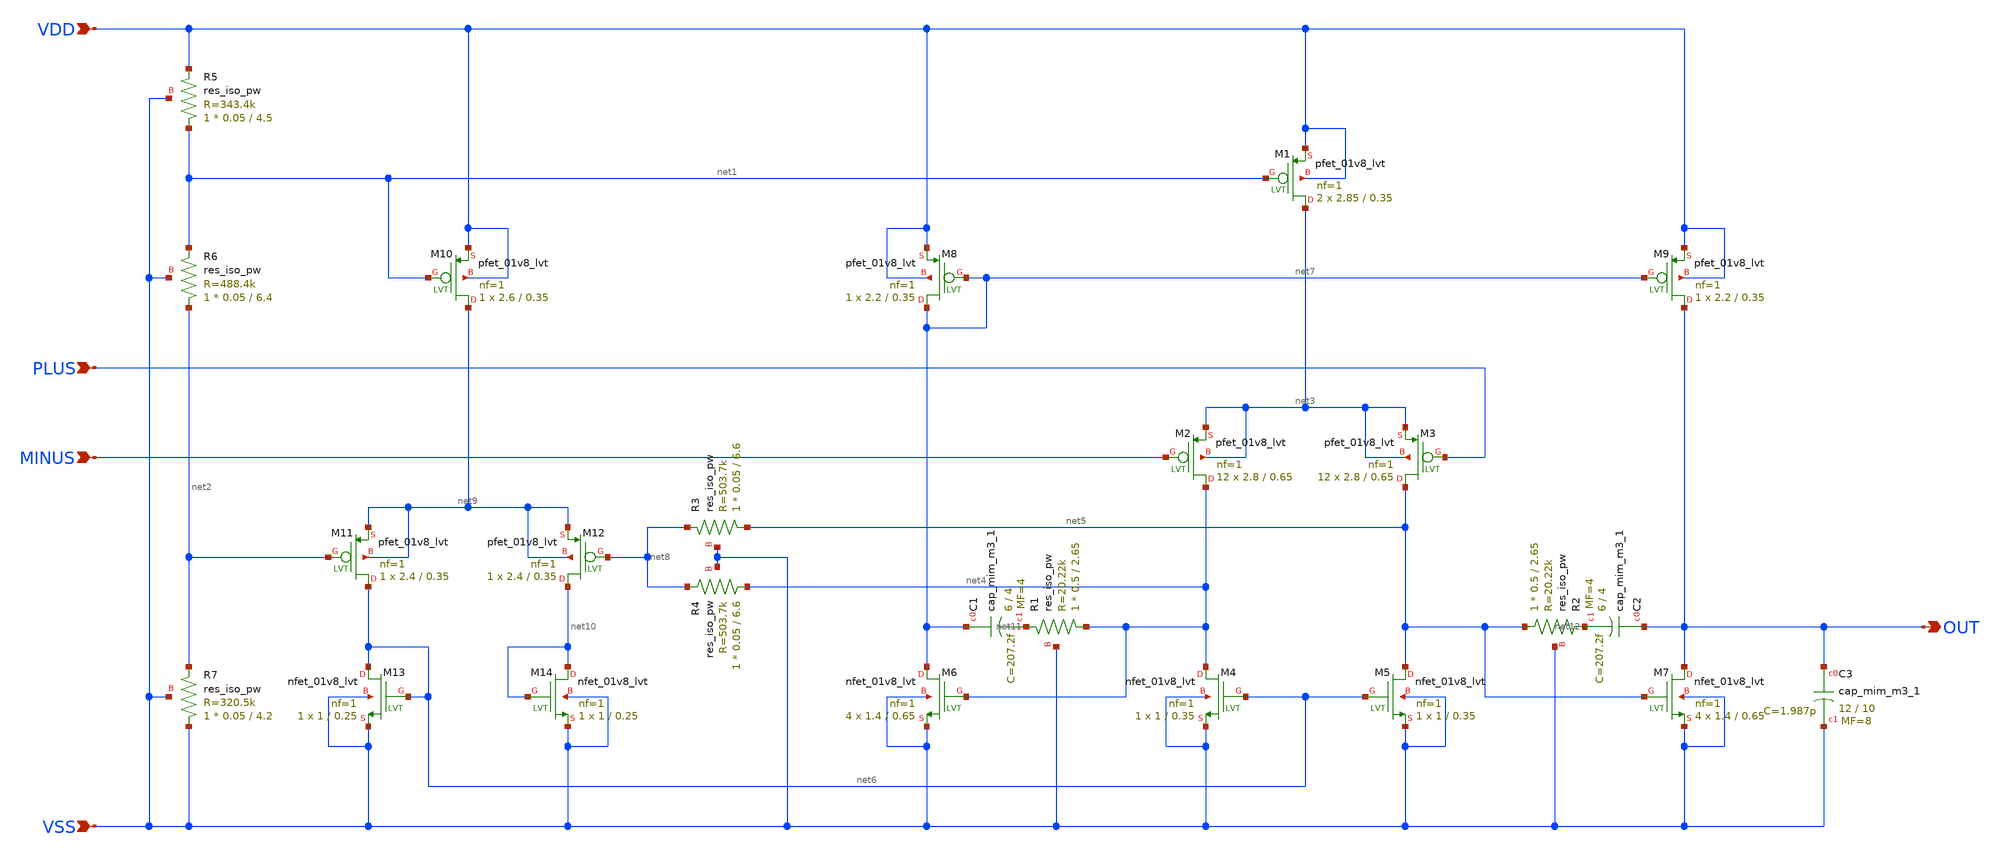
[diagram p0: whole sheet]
** sch_path: schematic/opamp.sch
**.subckt opamp VDD VSS PLUS MINUS OUT
*.ipin VDD
*.ipin VSS
*.ipin PLUS
*.ipin MINUS
*.opin OUT
XM1 net3 net1 VDD VDD sky130_fd_pr__pfet_01v8_lvt L=0.35 W=2.85 nf=1 ad='int((1 + 1)/2) * 2.85 / 1 * 0.29'
+ as='int((1 + 2)/2) * 2.85 / 1 * 0.29' pd='2*int((1 + 1)/2) * (2.85 / 1 + 0.29)' ps='2*int((1 + 2)/2) * (2.85 / 1 + 0.29)'
+ nrd='0.29 / 2.85 ' nrs='0.29 / 2.85 ' sa=0 sb=0 sd=0 mult=2 m=2
XM2 net4 MINUS net3 net3 sky130_fd_pr__pfet_01v8_lvt L=0.65 W=2.8 nf=1 ad='int((1 + 1)/2) * 2.8 / 1 * 0.29'
+ as='int((1 + 2)/2) * 2.8 / 1 * 0.29' pd='2*int((1 + 1)/2) * (2.8 / 1 + 0.29)' ps='2*int((1 + 2)/2) * (2.8 / 1 + 0.29)'
+ nrd='0.29 / 2.8 ' nrs='0.29 / 2.8 ' sa=0 sb=0 sd=0 mult=12 m=12
XM3 net5 PLUS net3 net3 sky130_fd_pr__pfet_01v8_lvt L=0.65 W=2.8 nf=1 ad='int((1 + 1)/2) * 2.8 / 1 * 0.29'
+ as='int((1 + 2)/2) * 2.8 / 1 * 0.29' pd='2*int((1 + 1)/2) * (2.8 / 1 + 0.29)' ps='2*int((1 + 2)/2) * (2.8 / 1 + 0.29)'
+ nrd='0.29 / 2.8 ' nrs='0.29 / 2.8 ' sa=0 sb=0 sd=0 mult=12 m=12
XM4 net4 net6 VSS VSS sky130_fd_pr__nfet_01v8_lvt L=0.35 W=1 nf=1 ad='int((1 + 1)/2) * 1 / 1 * 0.29'
+ as='int((1 + 2)/2) * 1 / 1 * 0.29' pd='2*int((1 + 1)/2) * (1 / 1 + 0.29)' ps='2*int((1 + 2)/2) * (1 / 1 + 0.29)'
+ nrd='0.29 / 1 ' nrs='0.29 / 1 ' sa=0 sb=0 sd=0 mult=1 m=1
XM5 net5 net6 VSS VSS sky130_fd_pr__nfet_01v8_lvt L=0.35 W=1 nf=1 ad='int((1 + 1)/2) * 1 / 1 * 0.29'
+ as='int((1 + 2)/2) * 1 / 1 * 0.29' pd='2*int((1 + 1)/2) * (1 / 1 + 0.29)' ps='2*int((1 + 2)/2) * (1 / 1 + 0.29)'
+ nrd='0.29 / 1 ' nrs='0.29 / 1 ' sa=0 sb=0 sd=0 mult=1 m=1
XM6 net7 net4 VSS VSS sky130_fd_pr__nfet_01v8_lvt L=0.65 W=1.4 nf=1 ad='int((1 + 1)/2) * 1.4 / 1 * 0.29'
+ as='int((1 + 2)/2) * 1.4 / 1 * 0.29' pd='2*int((1 + 1)/2) * (1.4 / 1 + 0.29)' ps='2*int((1 + 2)/2) * (1.4 / 1 + 0.29)'
+ nrd='0.29 / 1.4 ' nrs='0.29 / 1.4 ' sa=0 sb=0 sd=0 mult=4 m=4
XM7 OUT net5 VSS VSS sky130_fd_pr__nfet_01v8_lvt L=0.65 W=1.4 nf=1 ad='int((1 + 1)/2) * 1.4 / 1 * 0.29'
+ as='int((1 + 2)/2) * 1.4 / 1 * 0.29' pd='2*int((1 + 1)/2) * (1.4 / 1 + 0.29)' ps='2*int((1 + 2)/2) * (1.4 / 1 + 0.29)'
+ nrd='0.29 / 1.4 ' nrs='0.29 / 1.4 ' sa=0 sb=0 sd=0 mult=4 m=4
XM8 net7 net7 VDD VDD sky130_fd_pr__pfet_01v8_lvt L=0.35 W=2.2 nf=1 ad='int((1 + 1)/2) * 2.2 / 1 * 0.29'
+ as='int((1 + 2)/2) * 2.2 / 1 * 0.29' pd='2*int((1 + 1)/2) * (2.2 / 1 + 0.29)' ps='2*int((1 + 2)/2) * (2.2 / 1 + 0.29)'
+ nrd='0.29 / 2.2 ' nrs='0.29 / 2.2 ' sa=0 sb=0 sd=0 mult=1 m=1
XM9 OUT net7 VDD VDD sky130_fd_pr__pfet_01v8_lvt L=0.35 W=2.2 nf=1 ad='int((1 + 1)/2) * 2.2 / 1 * 0.29'
+ as='int((1 + 2)/2) * 2.2 / 1 * 0.29' pd='2*int((1 + 1)/2) * (2.2 / 1 + 0.29)' ps='2*int((1 + 2)/2) * (2.2 / 1 + 0.29)'
+ nrd='0.29 / 2.2 ' nrs='0.29 / 2.2 ' sa=0 sb=0 sd=0 mult=1 m=1
XM10 net9 net1 VDD VDD sky130_fd_pr__pfet_01v8_lvt L=0.35 W=2.6 nf=1 ad='int((1 + 1)/2) * 2.6 / 1 * 0.29'
+ as='int((1 + 2)/2) * 2.6 / 1 * 0.29' pd='2*int((1 + 1)/2) * (2.6 / 1 + 0.29)' ps='2*int((1 + 2)/2) * (2.6 / 1 + 0.29)'
+ nrd='0.29 / 2.6 ' nrs='0.29 / 2.6 ' sa=0 sb=0 sd=0 mult=1 m=1
XM11 net6 net2 net9 net9 sky130_fd_pr__pfet_01v8_lvt L=0.35 W=2.4 nf=1 ad='int((1 + 1)/2) * 2.4 / 1 * 0.29'
+ as='int((1 + 2)/2) * 2.4 / 1 * 0.29' pd='2*int((1 + 1)/2) * (2.4 / 1 + 0.29)' ps='2*int((1 + 2)/2) * (2.4 / 1 + 0.29)'
+ nrd='0.29 / 2.4 ' nrs='0.29 / 2.4 ' sa=0 sb=0 sd=0 mult=1 m=1
XM12 net10 net8 net9 net9 sky130_fd_pr__pfet_01v8_lvt L=0.35 W=2.4 nf=1 ad='int((1 + 1)/2) * 2.4 / 1 * 0.29'
+ as='int((1 + 2)/2) * 2.4 / 1 * 0.29' pd='2*int((1 + 1)/2) * (2.4 / 1 + 0.29)' ps='2*int((1 + 2)/2) * (2.4 / 1 + 0.29)'
+ nrd='0.29 / 2.4 ' nrs='0.29 / 2.4 ' sa=0 sb=0 sd=0 mult=1 m=1
XM13 net6 net6 VSS VSS sky130_fd_pr__nfet_01v8_lvt L=0.25 W=1 nf=1 ad='int((1 + 1)/2) * 1 / 1 * 0.29'
+ as='int((1 + 2)/2) * 1 / 1 * 0.29' pd='2*int((1 + 1)/2) * (1 / 1 + 0.29)' ps='2*int((1 + 2)/2) * (1 / 1 + 0.29)'
+ nrd='0.29 / 1 ' nrs='0.29 / 1 ' sa=0 sb=0 sd=0 mult=1 m=1
XM14 net10 net10 VSS VSS sky130_fd_pr__nfet_01v8_lvt L=0.25 W=1 nf=1 ad='int((1 + 1)/2) * 1 / 1 * 0.29'
+ as='int((1 + 2)/2) * 1 / 1 * 0.29' pd='2*int((1 + 1)/2) * (1 / 1 + 0.29)' ps='2*int((1 + 2)/2) * (1 / 1 + 0.29)'
+ nrd='0.29 / 1 ' nrs='0.29 / 1 ' sa=0 sb=0 sd=0 mult=1 m=1
XR1 net4 net11 VSS sky130_fd_pr__res_iso_pw W=0.5 L=2.65 m=1
XR2 net5 net12 VSS sky130_fd_pr__res_iso_pw W=0.5 L=2.65 m=1
XR3 net5 net8 VSS sky130_fd_pr__res_iso_pw W=0.05 L=6.6 m=1
XR4 net4 net8 VSS sky130_fd_pr__res_iso_pw W=0.05 L=6.6 m=1
XR5 net1 VDD VSS sky130_fd_pr__res_iso_pw W=0.05 L=4.5 m=1
XR6 net2 net1 VSS sky130_fd_pr__res_iso_pw W=0.05 L=6.4 m=1
XR7 VSS net2 VSS sky130_fd_pr__res_iso_pw W=0.05 L=4.2 m=1
XC1 net7 net11 sky130_fd_pr__cap_mim_m3_1 W=6 L=4 MF=4 m=4
XC2 OUT net12 sky130_fd_pr__cap_mim_m3_1 W=6 L=4 MF=4 m=4
XC3 OUT VSS sky130_fd_pr__cap_mim_m3_1 W=12 L=10 MF=8 m=8
**.ends
.end
